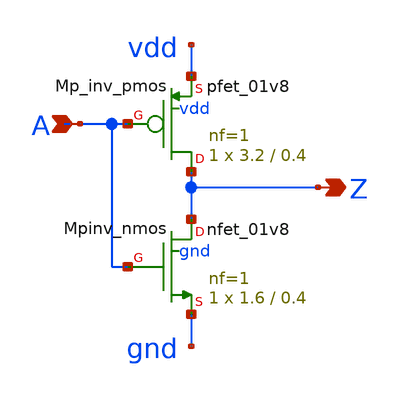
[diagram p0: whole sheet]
** sch_path: sram_2_64_scn4m_lcc/pinv_0.sch
**.subckt pinv_0 A Z
*.ipin A
*.opin Z
XMpinv_nmos Z A gnd gnd sky130_fd_pr__nfet_01v8 L=0.4 W=1.6 nf=1 ad='int((nf+1)/2) * W/nf * 0.29' as='int((nf+2)/2) * W/nf * 0.29'
+ pd='2*int((nf+1)/2) * (W/nf + 0.29)' ps='2*int((nf+2)/2) * (W/nf + 0.29)' nrd='0.29 / W' nrs='0.29 / W'
+ sa=0 sb=0 sd=0 mult=1 m=1
XMp_inv_pmos Z A vdd vdd sky130_fd_pr__pfet_01v8 L=0.4 W=3.2 nf=1 ad='int((nf+1)/2) * W/nf * 0.29' as='int((nf+2)/2) * W/nf * 0.29'
+ pd='2*int((nf+1)/2) * (W/nf + 0.29)' ps='2*int((nf+2)/2) * (W/nf + 0.29)' nrd='0.29 / W' nrs='0.29 / W'
+ sa=0 sb=0 sd=0 mult=1 m=1
**.ends
.end
